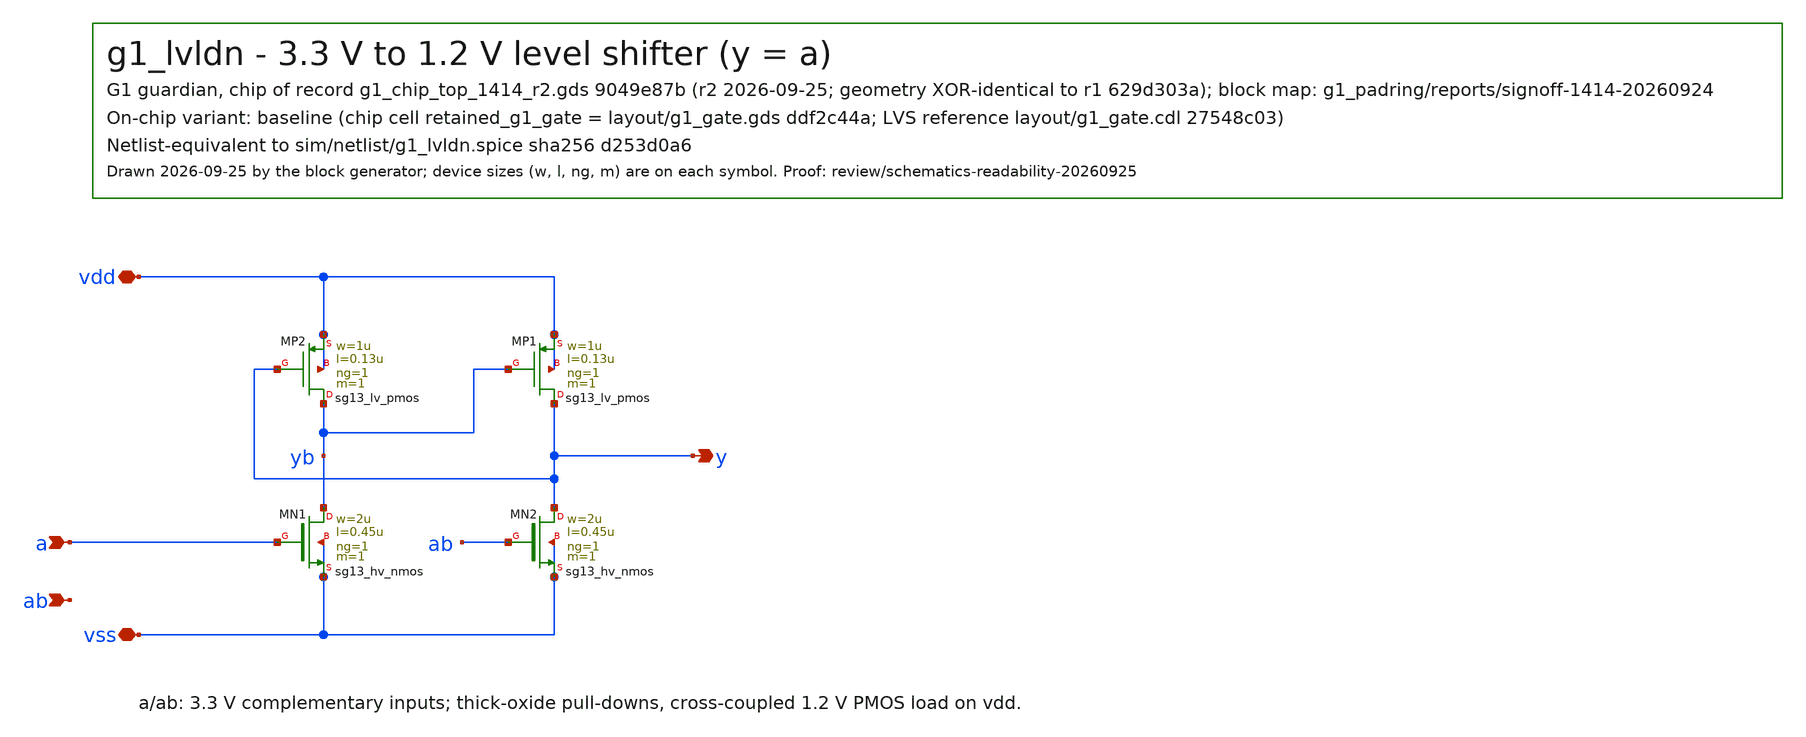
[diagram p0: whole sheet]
** sch_path: designs/g1-guardian/blocks/g1_gate/schematic/g1_lvldn.sch
**.subckt g1_lvldn a ab y vdd vss
*.ipin a
*.ipin ab
*.opin y
*.iopin vdd
*.iopin vss
XMN1 yb a vss vss sg13_hv_nmos w=2u l=0.45u ng=1 m=1 mm_ok=1
XMN2 y ab vss vss sg13_hv_nmos w=2u l=0.45u ng=1 m=1 mm_ok=1
XMP1 y yb vdd vdd sg13_lv_pmos w=1u l=0.13u ng=1 m=1 mm_ok=1
XMP2 yb y vdd vdd sg13_lv_pmos w=1u l=0.13u ng=1 m=1 mm_ok=1
**.ends
.end
